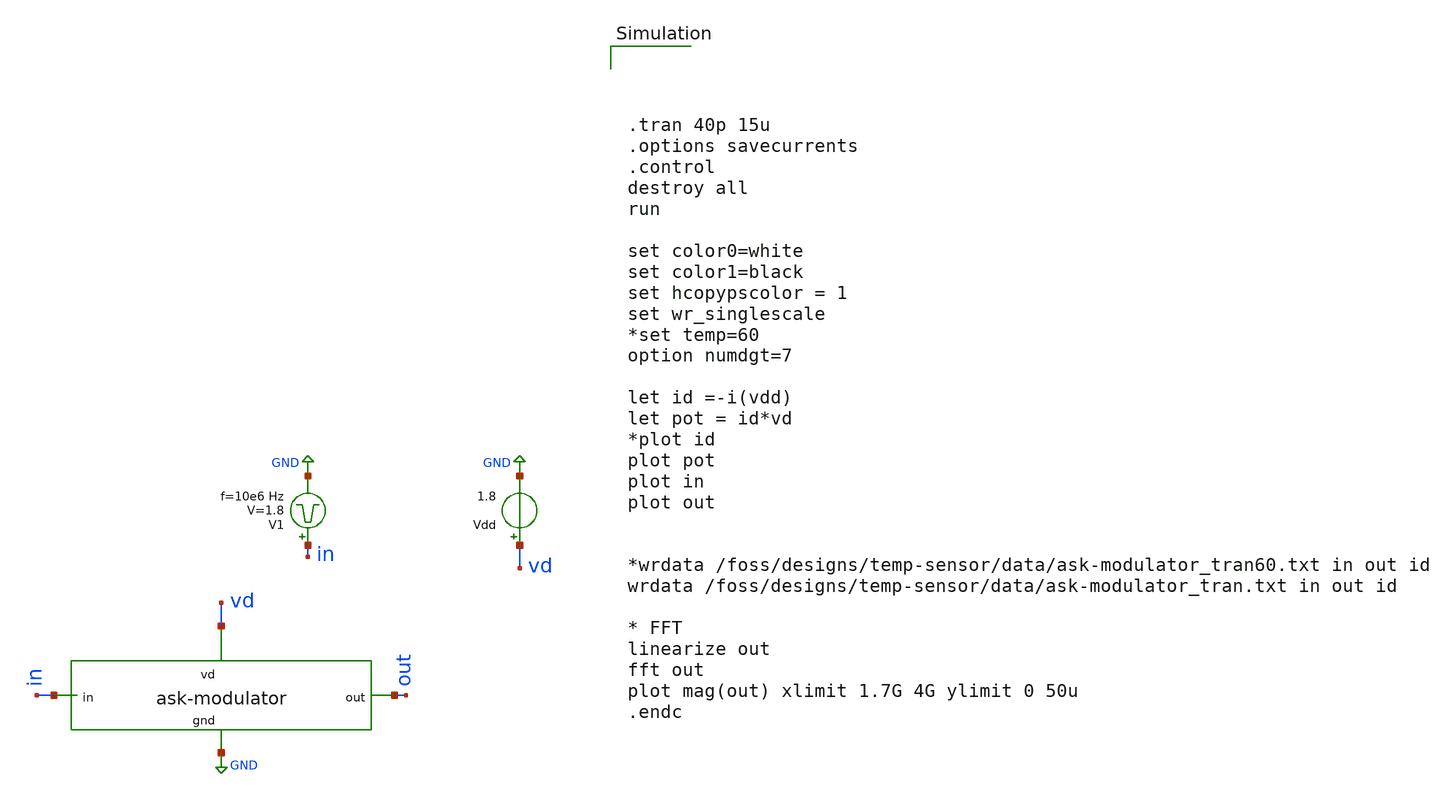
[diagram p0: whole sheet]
** sch_path: ask_modulator/xschem/ask-modulator_tb-tran.sch
**.subckt ask-modulator_tb-tran
Vdd vd GND 1.8
V1 in GND pulse 0 1.8 '0.495/ 10e6 ' '0.01/10e6 ' '0.01/10e6 ' '0.49/10e6 ' '1/10e6 '
x1 vd out in GND ask-modulator
**** begin user architecture code




.tran 40p 15u
.options savecurrents
.control
destroy all
run

set color0=white
set color1=black
set hcopypscolor = 1
set wr_singlescale
*set temp=60
option numdgt=7

let id =-i(vdd)
let pot = id*vd
*plot id
plot pot
plot in
plot out


*wrdata /foss/designs/temp-sensor/data/ask-modulator_tran60.txt in out id
wrdata /foss/designs/temp-sensor/data/ask-modulator_tran.txt in out id

* FFT
linearize out
fft out
plot mag(out) xlimit 1.7G 4G ylimit 0 50u
.endc

 .lib $::SKYWATER_MODELS/sky130.lib.spice tt
.include $::SKYWATER_STDCELLS/sky130_fd_sc_hd.spice

**** end user architecture code
**.ends
.GLOBAL GND
.end
